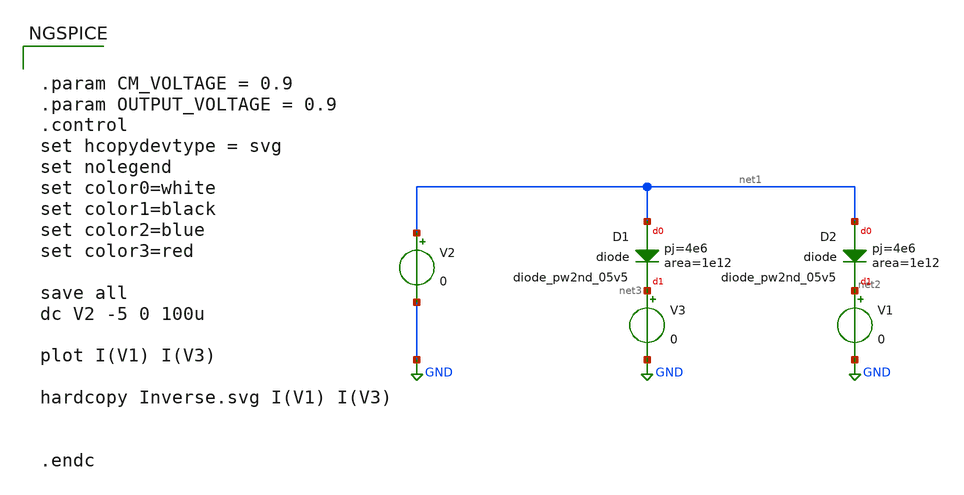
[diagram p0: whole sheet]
** sch_path: analog/xschem/Diode_Dtemp_PDK_tb.sch
**.subckt Diode_Dtemp_PDK_tb
V2 net1 GND 0
V1 net2 GND 0
V3 net3 GND 0
XD1 net1 net3 sky130_fd_pr__diode_pw2nd_05v5 area=1e12 pj=4e6
XD2 net1 net2 sky130_fd_pr__diode_pw2nd_05v5 area=1e12 pj=4e6
**** begin user architecture code


.param CM_VOLTAGE = 0.9
.param OUTPUT_VOLTAGE = 0.9
.control
set hcopydevtype = svg
set nolegend
set color0=white
set color1=black
set color2=blue
set color3=red

save all
dc V2 -5 0 100u

plot I(V1) I(V3)

hardcopy Inverse.svg I(V1) I(V3)


.endc



*.lib $::SKYWATER_MODELS/models/sky130.lib.spice tt
.lib /home/icarosix/asic/pdks/sky130A/libs.tech/ngspice/sky130.lib.spice tt
.option wnflag=1

**** end user architecture code
**.ends
.GLOBAL GND
**** begin user architecture code
[sky130_models]
**** end user architecture code
.end
